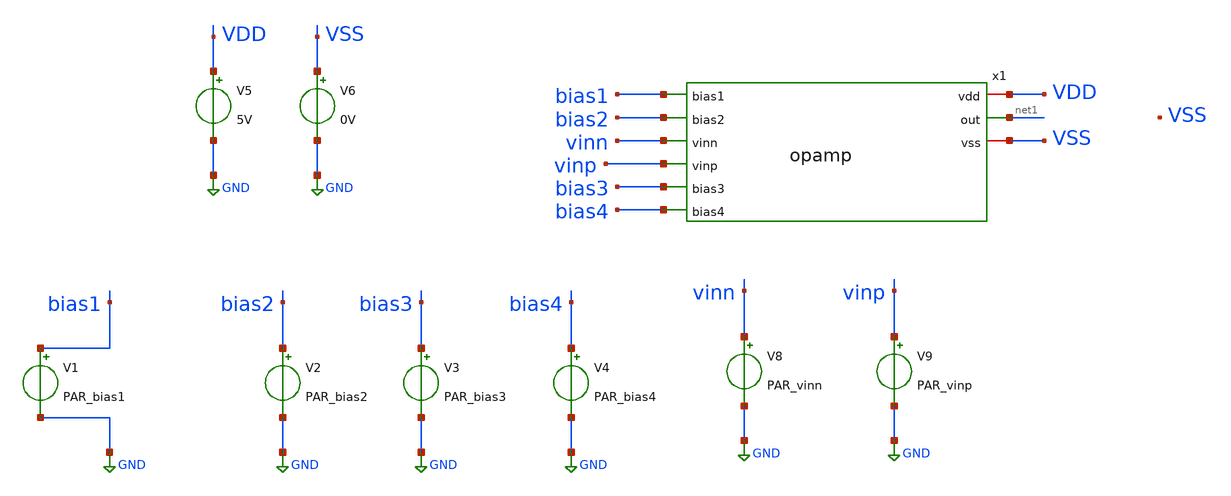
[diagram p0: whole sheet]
** sch_path: activities/opamp2AKAM/testBenchOpamp.sch
**.subckt testBenchOpamp
V1 bias1 GND PAR_bias1
V2 bias2 GND PAR_bias2
V3 bias3 GND PAR_bias3
V4 bias4 GND PAR_bias4
V5 VDD GND 5V
V6 VSS GND 0V
x1 VDD bias1 bias2 vinn net1 vinp bias3 bias4 VSS opamp
V8 vinn GND PAR_vinn
V9 vinp GND PAR_vinp
**.ends
.GLOBAL GND
.end
